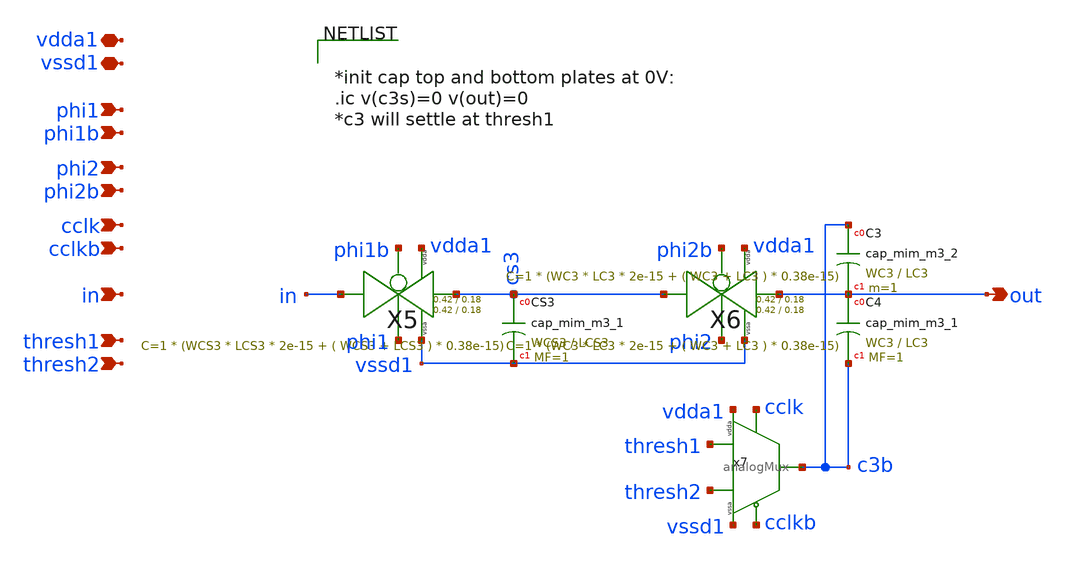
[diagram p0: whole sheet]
** sch_path: xschem/Switched_Caps/archive/2switchcaps_thresh.sch
**.subckt 2switchcaps_thresh phi1 phi1b thresh1 thresh2 out phi2 phi2b cclk cclkb in vdda1 vssd1
*.ipin phi1
*.ipin phi1b
*.ipin thresh1
*.ipin thresh2
*.opin out
*.ipin phi2
*.ipin phi2b
*.ipin cclk
*.ipin cclkb
*.ipin in
*.iopin vdda1
*.iopin vssd1
XC3 c3b out sky130_fd_pr__cap_mim_m3_2 W=WC3 L=LC3 MF=1 m=1
XCS3 cs3 vssd1 sky130_fd_pr__cap_mim_m3_1 W=WCS3 L=LCS3 MF=1 m=1
XC4 out c3b sky130_fd_pr__cap_mim_m3_1 W=WC3 L=LC3 MF=1 m=1
x7 thresh2 thresh1 cclk cclkb c3b vssd1 vdda1 analogMux
X5 in cs3 phi1b phi1 vdda1 vssd1 transmission_gate Wpmos=0.42 Lpmos=0.18 Wnmos=0.42 Lnmos=0.18
X6 cs3 out phi2b phi2 vdda1 vssd1 transmission_gate Wpmos=0.42 Lpmos=0.18 Wnmos=0.42 Lnmos=0.18
**** begin user architecture code


*init cap top and bottom plates at 0V:
.ic v(c3s)=0 v(out)=0
*c3 will settle at thresh1


**** end user architecture code
**.ends

* expanding   symbol:  mux/analogMux.sym # of pins=7
** sym_path: xschem/mux/analogMux.sym
** sch_path: xschem/mux/analogMux.sch
.subckt analogMux vref2 vref1 c cbar out vssa vdda
*.ipin vref1
*.opin out
*.ipin vref2
*.ipin c
*.ipin cbar
*.ipin vssa
*.ipin vdda
XM2 vref1 c out vssa sky130_fd_pr__nfet_01v8 L=0.15 W=0.42 nf=1 ad='int((nf+1)/2) * W/nf * 0.29' as='int((nf+2)/2) * W/nf * 0.29'
+ pd='2*int((nf+1)/2) * (W/nf + 0.29)' ps='2*int((nf+2)/2) * (W/nf + 0.29)' nrd='0.29 / W' nrs='0.29 / W'
+ sa=0 sb=0 sd=0 mult=1 m=1
XM4 vref1 cbar out vdda sky130_fd_pr__pfet_01v8 L=0.15 W=0.42 nf=1 ad='int((nf+1)/2) * W/nf * 0.29' as='int((nf+2)/2) * W/nf * 0.29'
+ pd='2*int((nf+1)/2) * (W/nf + 0.29)' ps='2*int((nf+2)/2) * (W/nf + 0.29)' nrd='0.29 / W' nrs='0.29 / W'
+ sa=0 sb=0 sd=0 mult=1 m=1
XM7 out cbar vref2 vssa sky130_fd_pr__nfet_01v8 L=0.15 W=0.42 nf=1 ad='int((nf+1)/2) * W/nf * 0.29' as='int((nf+2)/2) * W/nf * 0.29'
+ pd='2*int((nf+1)/2) * (W/nf + 0.29)' ps='2*int((nf+2)/2) * (W/nf + 0.29)' nrd='0.29 / W' nrs='0.29 / W'
+ sa=0 sb=0 sd=0 mult=1 m=1
XM8 out c vref2 vdda sky130_fd_pr__pfet_01v8 L=0.15 W=0.42 nf=1 ad='int((nf+1)/2) * W/nf * 0.29' as='int((nf+2)/2) * W/nf * 0.29'
+ pd='2*int((nf+1)/2) * (W/nf + 0.29)' ps='2*int((nf+2)/2) * (W/nf + 0.29)' nrd='0.29 / W' nrs='0.29 / W'
+ sa=0 sb=0 sd=0 mult=1 m=1
.ends


* expanding   symbol:  transmission_gate/transmission_gate.sym # of pins=6
** sym_path: xschem/transmission_gate/transmission_gate.sym
** sch_path: xschem/transmission_gate/transmission_gate.sch
.subckt transmission_gate in out ctrl_ ctrl vdda vssa  Wpmos=Wpmos Lpmos=Lpmos Wnmos=Wnmos
+ Lnmos=Lnmos
*.iopin in
*.iopin out
*.ipin ctrl_
*.ipin ctrl
*.ipin vdda
*.ipin vssa
XM1 out ctrl in vssa sky130_fd_pr__nfet_01v8 L=Lnmos W=Wnmos nf=1 ad='int((nf+1)/2) * W/nf * 0.29' as='int((nf+2)/2) * W/nf * 0.29'
+ pd='2*int((nf+1)/2) * (W/nf + 0.29)' ps='2*int((nf+2)/2) * (W/nf + 0.29)' nrd='0.29 / W' nrs='0.29 / W'
+ sa=0 sb=0 sd=0 mult=1 m=1
XM2 out ctrl_ in vdda sky130_fd_pr__pfet_01v8 L=Lpmos W=1.26 nf=1 ad='int((nf+1)/2) * W/nf * 0.29' as='int((nf+2)/2) * W/nf * 0.29'
+ pd='2*int((nf+1)/2) * (W/nf + 0.29)' ps='2*int((nf+2)/2) * (W/nf + 0.29)' nrd='0.29 / W' nrs='0.29 / W'
+ sa=0 sb=0 sd=0 mult=1 m=1
.ends

.end
